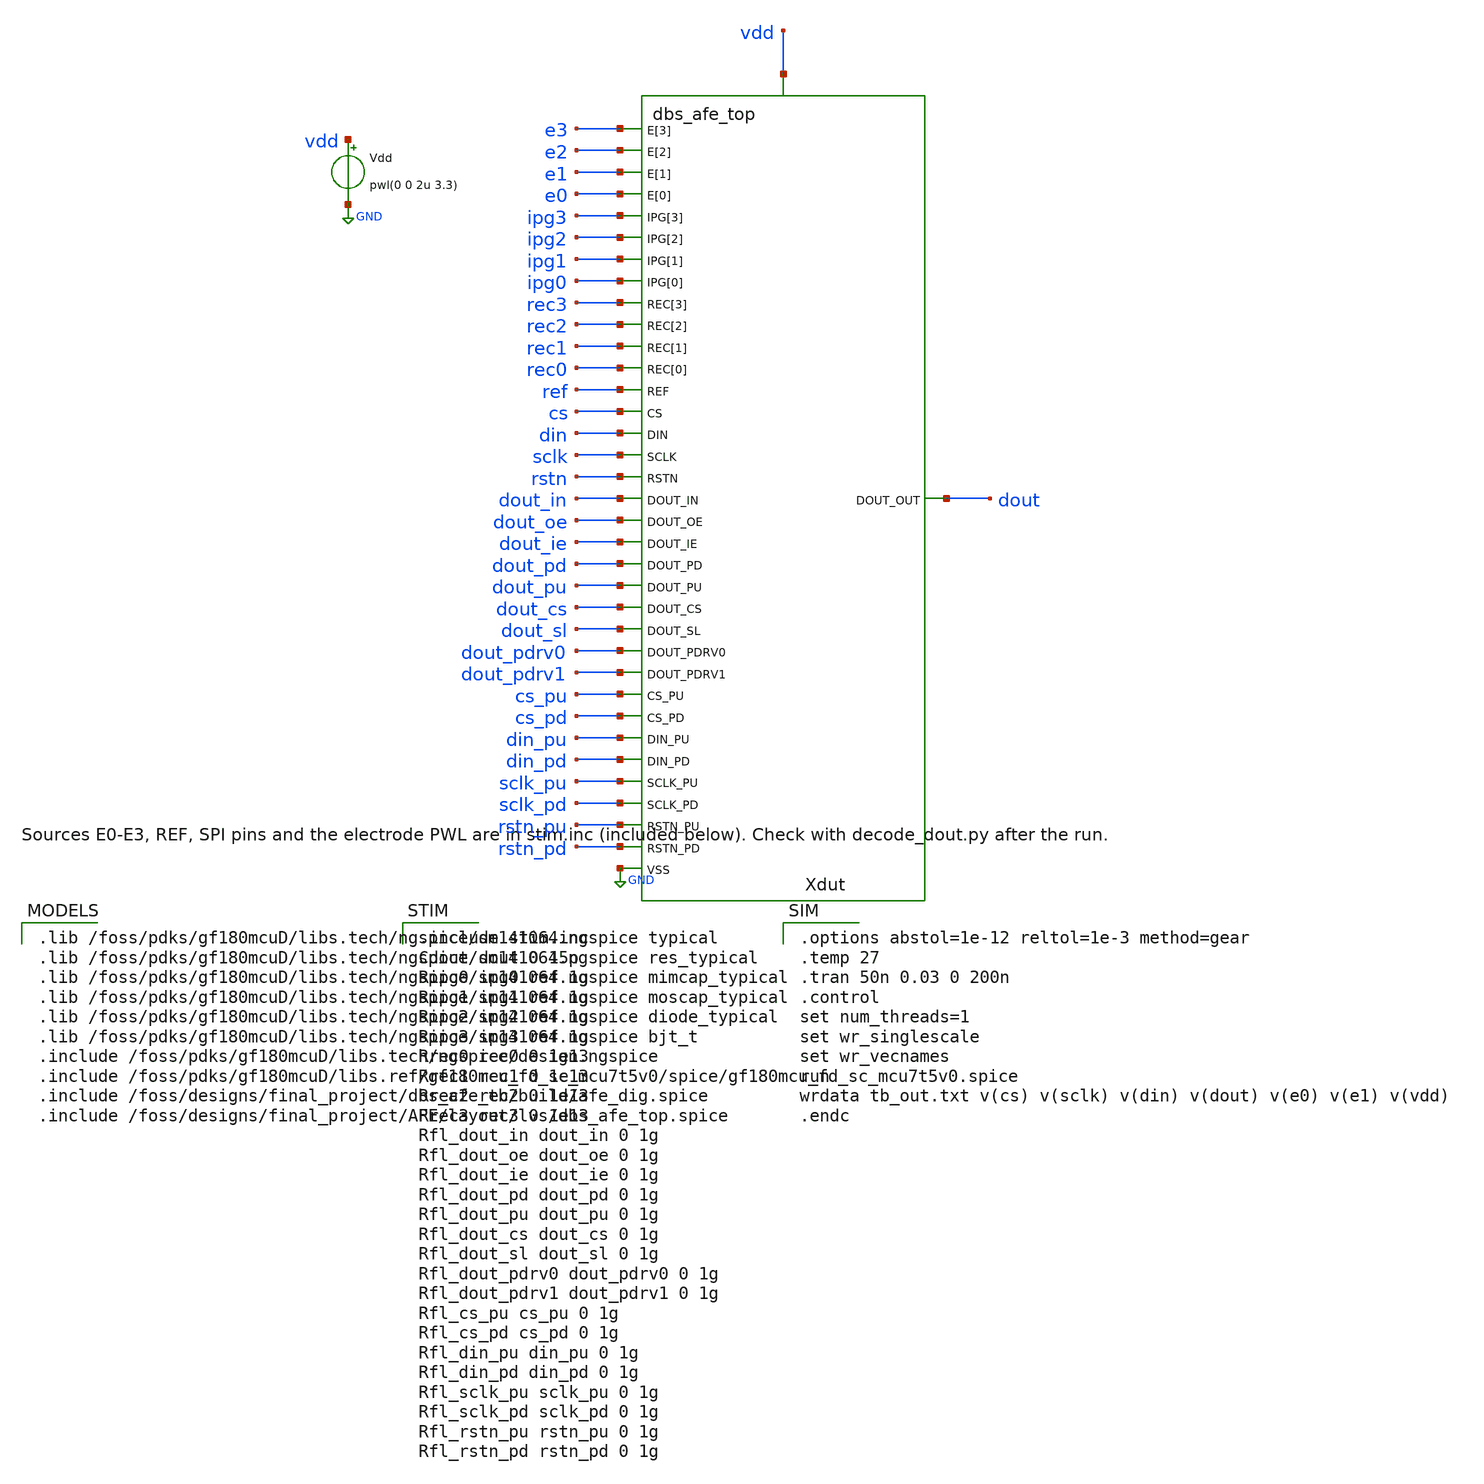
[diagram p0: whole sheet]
** sch_path: dbs_afe_tb/build/tb_dbs_afe_top.sch
**.subckt tb_dbs_afe_top
Xdut e3 e2 e1 e0 ipg3 ipg2 ipg1 ipg0 rec3 rec2 rec1 rec0 ref cs din sclk rstn dout dout_in dout_oe
+ dout_ie dout_pd dout_pu dout_cs dout_sl dout_pdrv0 dout_pdrv1 cs_pu cs_pd din_pu din_pd sclk_pu sclk_pd
+ rstn_pu rstn_pd vdd GND dbs_afe_top
Vdd vdd GND pwl(0 0 2u 3.3)
**** begin user architecture code

.lib /foss/pdks/gf180mcuD/libs.tech/ngspice/sm141064.ngspice typical
.lib /foss/pdks/gf180mcuD/libs.tech/ngspice/sm141064.ngspice res_typical
.lib /foss/pdks/gf180mcuD/libs.tech/ngspice/sm141064.ngspice mimcap_typical
.lib /foss/pdks/gf180mcuD/libs.tech/ngspice/sm141064.ngspice moscap_typical
.lib /foss/pdks/gf180mcuD/libs.tech/ngspice/sm141064.ngspice diode_typical
.lib /foss/pdks/gf180mcuD/libs.tech/ngspice/sm141064.ngspice bjt_t
.include /foss/pdks/gf180mcuD/libs.tech/ngspice/design.ngspice
.include /foss/pdks/gf180mcuD/libs.ref/gf180mcu_fd_sc_mcu7t5v0/spice/gf180mcu_fd_sc_mcu7t5v0.spice
.include /foss/designs/final_project/dbs_afe_tb/build/afe_dig.spice
.include /foss/designs/final_project/AFE/layout/lvs/dbs_afe_top.spice


.include stim.inc
Cdout dout 0 15p
Ripg0 ipg0 ref 1g
Ripg1 ipg1 ref 1g
Ripg2 ipg2 ref 1g
Ripg3 ipg3 ref 1g
Rrec0 rec0 0 1e13
Rrec1 rec1 0 1e13
Rrec2 rec2 0 1e13
Rrec3 rec3 0 1e13
Rfl_dout_in dout_in 0 1g
Rfl_dout_oe dout_oe 0 1g
Rfl_dout_ie dout_ie 0 1g
Rfl_dout_pd dout_pd 0 1g
Rfl_dout_pu dout_pu 0 1g
Rfl_dout_cs dout_cs 0 1g
Rfl_dout_sl dout_sl 0 1g
Rfl_dout_pdrv0 dout_pdrv0 0 1g
Rfl_dout_pdrv1 dout_pdrv1 0 1g
Rfl_cs_pu cs_pu 0 1g
Rfl_cs_pd cs_pd 0 1g
Rfl_din_pu din_pu 0 1g
Rfl_din_pd din_pd 0 1g
Rfl_sclk_pu sclk_pu 0 1g
Rfl_sclk_pd sclk_pd 0 1g
Rfl_rstn_pu rstn_pu 0 1g
Rfl_rstn_pd rstn_pd 0 1g


.options abstol=1e-12 reltol=1e-3 method=gear
.temp 27
.tran 50n 0.03 0 200n
.control
set num_threads=1
set wr_singlescale
set wr_vecnames
run
wrdata tb_out.txt v(cs) v(sclk) v(din) v(dout) v(e0) v(e1) v(vdd)
.endc

**** end user architecture code
**.ends
.GLOBAL GND
.end
